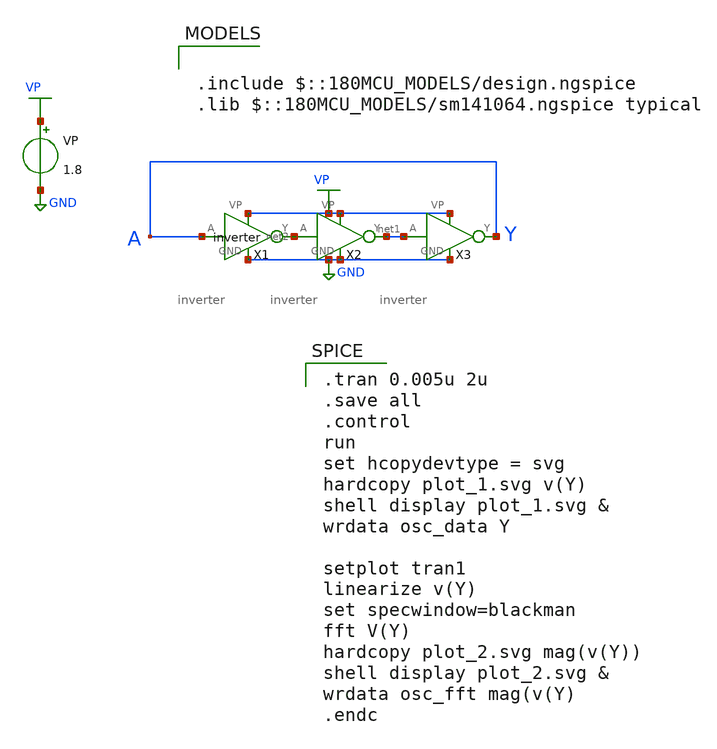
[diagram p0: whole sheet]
** sch_path: Designs/TopLevel_oscillator.sch
**.subckt TopLevel_oscillator
VP VP GND 1.8
X2 VP GND net1 net2 inverter
X1 VP GND net2 Y inverter
X3 VP GND Y net1 inverter
**** begin user architecture code

.include $::180MCU_MODELS/design.ngspice
.lib $::180MCU_MODELS/sm141064.ngspice typical


.tran 0.005u 2u
.save all
.control
run
set hcopydevtype = svg
hardcopy plot_1.svg v(Y)
shell display plot_1.svg &
wrdata osc_data Y

setplot tran1
linearize v(Y)
set specwindow=blackman
fft V(Y)
hardcopy plot_2.svg mag(v(Y))
shell display plot_2.svg &
wrdata osc_fft mag(v(Y)
.endc

**** end user architecture code
**.ends

* expanding   symbol:  Designs/inverter.sym # of pins=4
** sym_path: Designs/inverter.sym
** sch_path: Designs/inverter.sch
.subckt inverter VP GND Y A
*.ipin A
*.iopin VP
*.iopin GND
*.opin Y
XM3 Y A VP VP pfet_03v3 L=5u W=0.5u nf=1 ad='int((nf+1)/2) * W/nf * 0.18u' as='int((nf+2)/2) * W/nf * 0.18u'
+ pd='2*int((nf+1)/2) * (W/nf + 0.18u)' ps='2*int((nf+2)/2) * (W/nf + 0.18u)' nrd='0.18u / W' nrs='0.18u / W'
+ sa=0 sb=0 sd=0 m=1
XM4 Y A GND GND nfet_03v3 L=5u W=0.5u nf=1 ad='int((nf+1)/2) * W/nf * 0.18u' as='int((nf+2)/2) * W/nf * 0.18u'
+ pd='2*int((nf+1)/2) * (W/nf + 0.18u)' ps='2*int((nf+2)/2) * (W/nf + 0.18u)' nrd='0.18u / W' nrs='0.18u / W'
+ sa=0 sb=0 sd=0 m=1
.ends

.GLOBAL GND
.GLOBAL VP
.end
